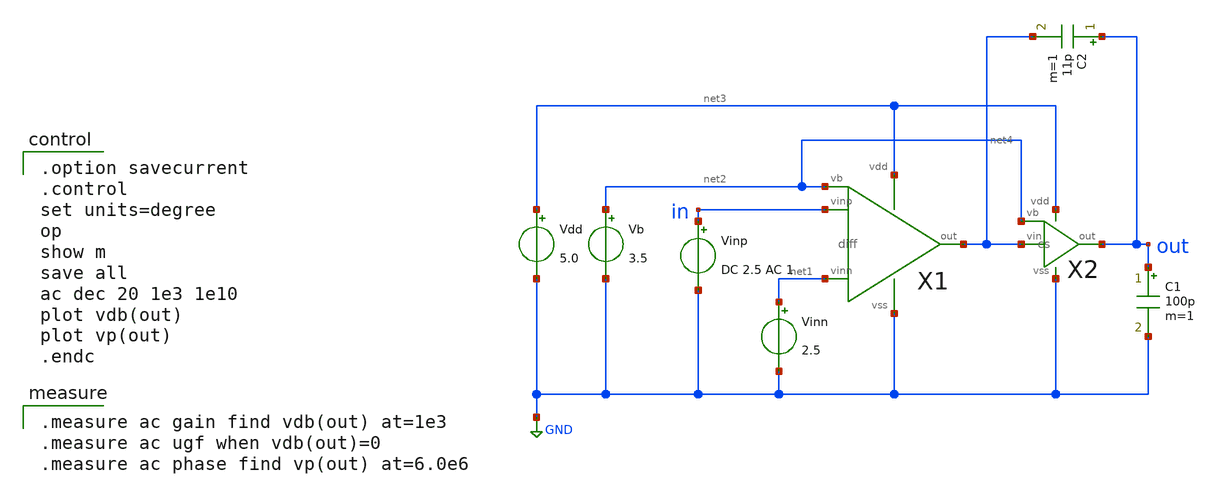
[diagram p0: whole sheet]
** sch_path: member_project/opamp/makoto645/testbench/2stage_cc_ac.sch
**.subckt 2stage_cc_ac
Vdd net3 GND 5.0
Vb net2 GND 3.5
Vinn net1 GND 2.5
Vinp in GND DC 2.5 AC 1
X1 in net1 net4 net3 GND net2 diff
X2 net4 net2 out net3 GND cs
C1 out GND 100p m=1
C2 out net4 11p m=1
**** begin user architecture code

.option savecurrent
.control
set units=degree
op
show m
save all
ac dec 20 1e3 1e10
plot vdb(out)
plot vp(out)
.endc


.measure ac gain find vdb(out) at=1e3
.measure ac ugf when vdb(out)=0
.measure ac phase find vp(out) at=6.0e6

 .include $::LIB/ip62_models
**** end user architecture code
**.ends

* expanding   symbol:  diff.sym # of pins=6
** sym_path: diff.sym
** sch_path: diff.sch
.subckt diff vinp vinn out vdd vss vb
*.ipin vinn
*.ipin vinp
*.ipin vb
*.opin out
*.iopin vdd
*.iopin vss
XM5 net2 vb vdd vdd PMOS w=200u l=2u as=0 ad=0 ps=0 pd=0 nrd=0 nrs=0 m=1
XM1 net1 vinn net2 net2 PMOS w=100u l=2u as=0 ad=0 ps=0 pd=0 nrd=0 nrs=0 m=1
XM2 out vinp net2 net2 PMOS w=100u l=2u as=0 ad=0 ps=0 pd=0 nrd=0 nrs=0 m=1
XM3 net1 net1 vss vss NMOS w=50u l=2u as=0 ad=0 ps=0 pd=0 nrd=0 nrs=0 m=1
XM4 out net1 vss vss NMOS w=50u l=2u as=0 ad=0 ps=0 pd=0 nrd=0 nrs=0 m=1
.ends


* expanding   symbol:  cs.sym # of pins=5
** sym_path: cs.sym
** sch_path: cs.sch
.subckt cs vin vb out vdd vss
*.ipin vb
*.ipin vin
*.opin out
*.iopin vss
*.iopin vdd
XM6 out vb vdd vdd PMOS w=480u l=2u as=0 ad=0 ps=0 pd=0 nrd=0 nrs=0 m=1
XM7 out vin vss vss NMOS w=220u l=2u as=0 ad=0 ps=0 pd=0 nrd=0 nrs=0 m=1
.ends

.GLOBAL GND
.end
